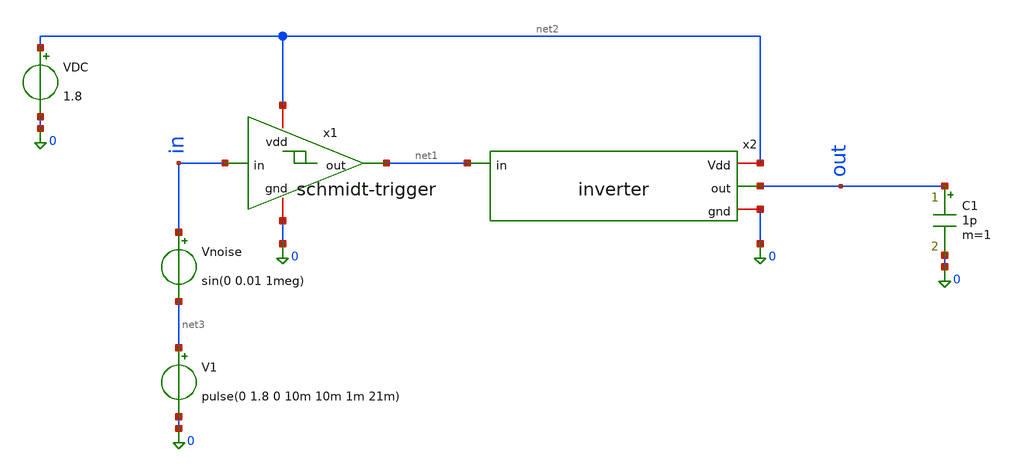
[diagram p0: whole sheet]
** sch_path: analog/mixer/schmidt-trigger-tb.sch
**.subckt schmidt-trigger-tb
x1 net2 net1 in 0 schmidt-trigger
VDC net2 0 1.8
V1 net3 0 pulse(0 1.8 0 10m 10m 1m 21m)
C1 out 0 1p m=1
Vnoise in net3 sin(0 0.01 1meg)
x2 net2 net1 out 0 inverter
**** begin user architecture code



.lib /usr/local/share/pdk/sky130A/libs.tech/ngspice/sky130.lib.spice tt



.control
    run
 tran 0.0001m 10m

    * Graficamos en el tiempo para ver el ruido (si lo dejaste activado)
    plot in out title 'Respuesta Temporal con Ruido'
.endc

.end


**** end user architecture code
**.ends

* expanding   symbol:  schmidt-trigger.sym # of pins=4
** sym_path: analog/mixer/schmidt-trigger.sym
** sch_path: analog/mixer/schmidt-trigger.sch
.subckt schmidt-trigger vdd out in gnd
*.opin out
*.ipin in
*.iopin vdd
*.iopin gnd
XM2 out in vdd vdd sky130_fd_pr__pfet_01v8 L=0.5 W=5 nf=1 ad='int((1 + 1)/2) * 5 / 1 * 0.29' as='int((1 + 2)/2) * 5 / 1 * 0.29'
+ pd='2*int((1 + 1)/2) * (5 / 1 + 0.29)' ps='2*int((1 + 2)/2) * (5 / 1 + 0.29)' nrd='0.29 / 5 ' nrs='0.29 / 5 '
+ sa=0 sb=0 sd=0 mult=1 m=1
XM1 vdd in vdd vdd sky130_fd_pr__pfet_01v8 L=1 W=6 nf=1 ad='int((1 + 1)/2) * 6 / 1 * 0.29' as='int((1 + 2)/2) * 6 / 1 * 0.29'
+ pd='2*int((1 + 1)/2) * (6 / 1 + 0.29)' ps='2*int((1 + 2)/2) * (6 / 1 + 0.29)' nrd='0.29 / 6 ' nrs='0.29 / 6 '
+ sa=0 sb=0 sd=0 mult=1 m=1
XM3 gnd out vdd vdd sky130_fd_pr__pfet_01v8 L=0.5 W=5 nf=1 ad='int((1 + 1)/2) * 5 / 1 * 0.29' as='int((1 + 2)/2) * 5 / 1 * 0.29'
+ pd='2*int((1 + 1)/2) * (5 / 1 + 0.29)' ps='2*int((1 + 2)/2) * (5 / 1 + 0.29)' nrd='0.29 / 5 ' nrs='0.29 / 5 '
+ sa=0 sb=0 sd=0 mult=1 m=1
XM4 out in gnd gnd sky130_fd_pr__nfet_01v8 L=0.5 W=1 nf=1 ad='int((1 + 1)/2) * 1 / 1 * 0.29' as='int((1 + 2)/2) * 1 / 1 * 0.29'
+ pd='2*int((1 + 1)/2) * (1 / 1 + 0.29)' ps='2*int((1 + 2)/2) * (1 / 1 + 0.29)' nrd='0.29 / 1 ' nrs='0.29 / 1 '
+ sa=0 sb=0 sd=0 mult=1 m=1
XM5 gnd in gnd gnd sky130_fd_pr__nfet_01v8 L=0.5 W=1 nf=1 ad='int((1 + 1)/2) * 1 / 1 * 0.29' as='int((1 + 2)/2) * 1 / 1 * 0.29'
+ pd='2*int((1 + 1)/2) * (1 / 1 + 0.29)' ps='2*int((1 + 2)/2) * (1 / 1 + 0.29)' nrd='0.29 / 1 ' nrs='0.29 / 1 '
+ sa=0 sb=0 sd=0 mult=1 m=1
XM6 vdd out gnd gnd sky130_fd_pr__nfet_01v8 L=0.5 W=1 nf=1 ad='int((1 + 1)/2) * 1 / 1 * 0.29' as='int((1 + 2)/2) * 1 / 1 * 0.29'
+ pd='2*int((1 + 1)/2) * (1 / 1 + 0.29)' ps='2*int((1 + 2)/2) * (1 / 1 + 0.29)' nrd='0.29 / 1 ' nrs='0.29 / 1 '
+ sa=0 sb=0 sd=0 mult=1 m=1
.ends


* expanding   symbol:  /home/jorge/VLSI-Projects/analog/tim-edwards-ws/inverter/xschem/inverter.sym
*+ # of pins=4
** sym_path: analog/tim-edwards-ws/inverter/xschem/inverter.sym
** sch_path: analog/tim-edwards-ws/inverter/xschem/inverter.sch
.subckt inverter Vdd in out gnd
*.ipin in
*.opin out
*.iopin gnd
*.iopin Vdd
XM1 out in gnd gnd sky130_fd_pr__nfet_01v8 L=0.5 W=1 nf=1 ad='int((1 + 1)/2) * 1 / 1 * 0.29' as='int((1 + 2)/2) * 1 / 1 * 0.29'
+ pd='2*int((1 + 1)/2) * (1 / 1 + 0.29)' ps='2*int((1 + 2)/2) * (1 / 1 + 0.29)' nrd='0.29 / 1 ' nrs='0.29 / 1 '
+ sa=0 sb=0 sd=0 mult=1 m=1
XM2 out in Vdd VDD sky130_fd_pr__pfet_01v8 L=0.5 W=5 nf=1 ad='int((1 + 1)/2) * 5 / 1 * 0.29' as='int((1 + 2)/2) * 5 / 1 * 0.29'
+ pd='2*int((1 + 1)/2) * (5 / 1 + 0.29)' ps='2*int((1 + 2)/2) * (5 / 1 + 0.29)' nrd='0.29 / 5 ' nrs='0.29 / 5 '
+ sa=0 sb=0 sd=0 mult=1 m=1
.ends

.end
